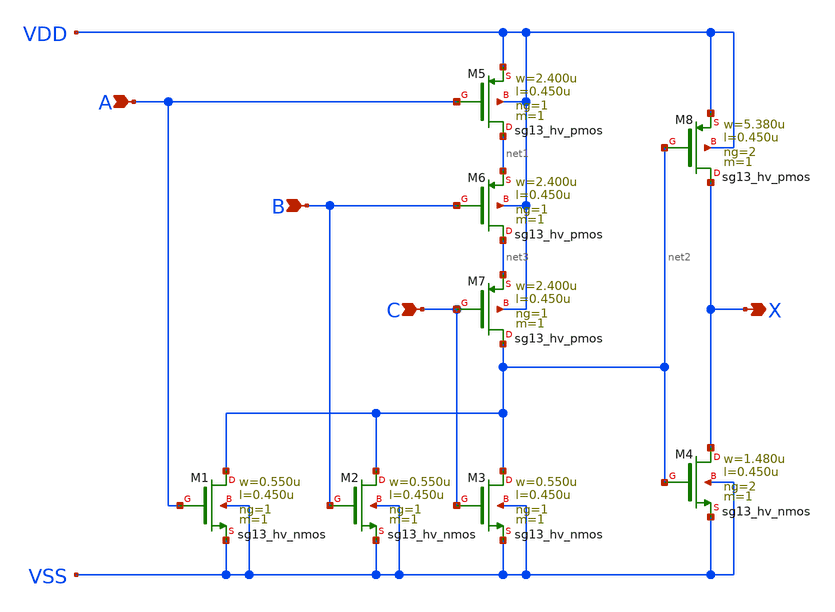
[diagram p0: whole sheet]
** sch_path: ihp-sg13g2/libs.ref/sg13g2_stdcell_hv/sch/xschem/sg13g2_hv_or3_2.sch
* Copyright 2023 IHP PDK Authors
* Licensed under the Apache License, Version 2.0 (the "License");
* you may not use this file except in compliance with the License.
* You may obtain a copy of the License at
* https://www.apache.org/licenses/LICENSE-2.0
* Unless required by applicable law or agreed to in writing, software
* distributed under the License is distributed on an "AS IS" BASIS,
* WITHOUT WARRANTIES OR CONDITIONS OF ANY KIND, either express or implied.
* See the License for the specific language governing permissions and
* limitations under the License.
**.subckt sg13g2_hv_or3_2 X C B A
*.opin X
*.ipin C
*.ipin B
*.ipin A
XM1 net2 A VSS VSS sg13_hv_nmos w=0.550u l=0.450u ng=1 m=1 mm_ok=1
XM2 net2 B VSS VSS sg13_hv_nmos w=0.550u l=0.450u ng=1 m=1 mm_ok=1
XM3 net2 C VSS VSS sg13_hv_nmos w=0.550u l=0.450u ng=1 m=1 mm_ok=1
XM4 X net2 VSS VSS sg13_hv_nmos w=1.480u l=0.450u ng=2 m=1 mm_ok=1
XM5 net1 A VDD VDD sg13_hv_pmos w=2.400u l=0.450u ng=1 m=1 mm_ok=1
XM6 net3 B net1 VDD sg13_hv_pmos w=2.400u l=0.450u ng=1 m=1 mm_ok=1
XM7 net2 C net3 VDD sg13_hv_pmos w=2.400u l=0.450u ng=1 m=1 mm_ok=1
XM8 X net2 VDD VDD sg13_hv_pmos w=5.380u l=0.450u ng=2 m=1 mm_ok=1
**.ends
.end
